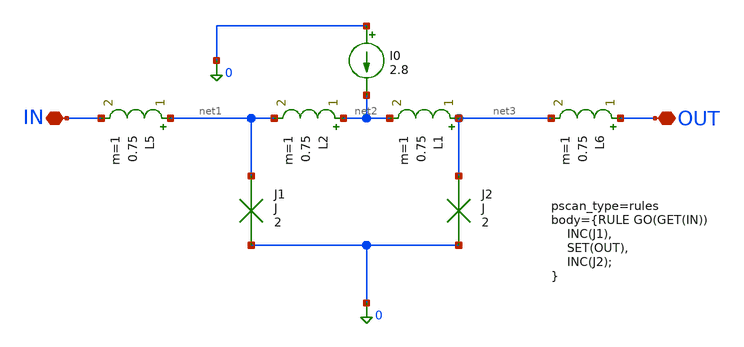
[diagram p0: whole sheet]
** sch_path: cells/jt2.sch
**.subckt jt2 OUT IN
*.iopin OUT
*.iopin IN
L1 net3 net2 0.75 m=1
L2 net2 net1 0.75 m=1
I0 0 net2 I?
L5 net1 IN 0.75 m=1
L6 OUT net3 0.75 m=1
J1 net1 0 J
J2 net3 0 J
**.ends
.end
